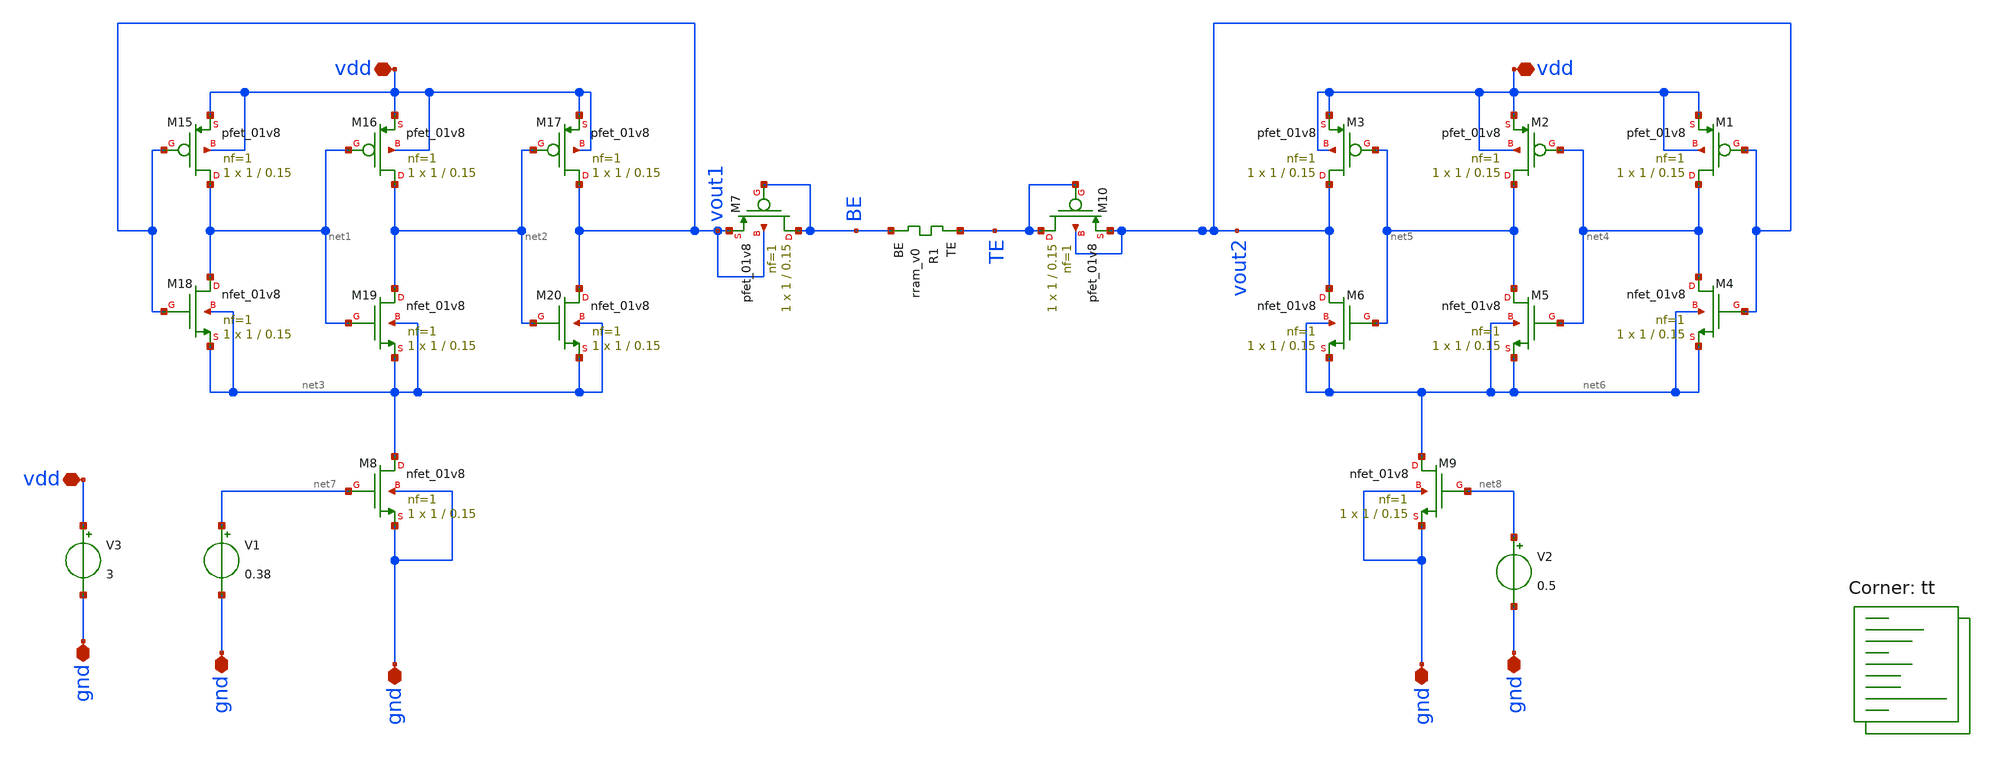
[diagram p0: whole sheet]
** sch_path: Neuron/voltContrOsc/sch/tb_vco_v2.sch
**.subckt tb_vco_v2 vdd vdd gnd gnd gnd gnd gnd vdd
*.iopin vdd
*.iopin vdd
*.iopin gnd
*.iopin gnd
*.iopin gnd
*.iopin gnd
*.iopin gnd
*.iopin vdd
XM15 net1 vout1 vdd vdd sky130_fd_pr__pfet_01v8 L=0.15 W=1 nf=1 ad='int((nf+1)/2) * W/nf * 0.29' as='int((nf+2)/2) * W/nf * 0.29'
+ pd='2*int((nf+1)/2) * (W/nf + 0.29)' ps='2*int((nf+2)/2) * (W/nf + 0.29)' nrd='0.29 / W' nrs='0.29 / W'
+ sa=0 sb=0 sd=0 mult=1 m=1
XM16 net2 net1 vdd vdd sky130_fd_pr__pfet_01v8 L=0.15 W=1 nf=1 ad='int((nf+1)/2) * W/nf * 0.29' as='int((nf+2)/2) * W/nf * 0.29'
+ pd='2*int((nf+1)/2) * (W/nf + 0.29)' ps='2*int((nf+2)/2) * (W/nf + 0.29)' nrd='0.29 / W' nrs='0.29 / W'
+ sa=0 sb=0 sd=0 mult=1 m=1
XM17 vout1 net2 vdd vdd sky130_fd_pr__pfet_01v8 L=0.15 W=1 nf=1 ad='int((nf+1)/2) * W/nf * 0.29' as='int((nf+2)/2) * W/nf * 0.29'
+ pd='2*int((nf+1)/2) * (W/nf + 0.29)' ps='2*int((nf+2)/2) * (W/nf + 0.29)' nrd='0.29 / W' nrs='0.29 / W'
+ sa=0 sb=0 sd=0 mult=1 m=1
XM18 net1 vout1 net3 net3 sky130_fd_pr__nfet_01v8 L=0.15 W=1 nf=1 ad='int((nf+1)/2) * W/nf * 0.29' as='int((nf+2)/2) * W/nf * 0.29'
+ pd='2*int((nf+1)/2) * (W/nf + 0.29)' ps='2*int((nf+2)/2) * (W/nf + 0.29)' nrd='0.29 / W' nrs='0.29 / W'
+ sa=0 sb=0 sd=0 mult=1 m=1
XM19 net2 net1 net3 net3 sky130_fd_pr__nfet_01v8 L=0.15 W=1 nf=1 ad='int((nf+1)/2) * W/nf * 0.29' as='int((nf+2)/2) * W/nf * 0.29'
+ pd='2*int((nf+1)/2) * (W/nf + 0.29)' ps='2*int((nf+2)/2) * (W/nf + 0.29)' nrd='0.29 / W' nrs='0.29 / W'
+ sa=0 sb=0 sd=0 mult=1 m=1
XM20 vout1 net2 net3 net3 sky130_fd_pr__nfet_01v8 L=0.15 W=1 nf=1 ad='int((nf+1)/2) * W/nf * 0.29' as='int((nf+2)/2) * W/nf * 0.29'
+ pd='2*int((nf+1)/2) * (W/nf + 0.29)' ps='2*int((nf+2)/2) * (W/nf + 0.29)' nrd='0.29 / W' nrs='0.29 / W'
+ sa=0 sb=0 sd=0 mult=1 m=1
XM1 net4 vout2 vdd vdd sky130_fd_pr__pfet_01v8 L=0.15 W=1 nf=1 ad='int((nf+1)/2) * W/nf * 0.29' as='int((nf+2)/2) * W/nf * 0.29'
+ pd='2*int((nf+1)/2) * (W/nf + 0.29)' ps='2*int((nf+2)/2) * (W/nf + 0.29)' nrd='0.29 / W' nrs='0.29 / W'
+ sa=0 sb=0 sd=0 mult=1 m=1
XM2 net5 net4 vdd vdd sky130_fd_pr__pfet_01v8 L=0.15 W=1 nf=1 ad='int((nf+1)/2) * W/nf * 0.29' as='int((nf+2)/2) * W/nf * 0.29'
+ pd='2*int((nf+1)/2) * (W/nf + 0.29)' ps='2*int((nf+2)/2) * (W/nf + 0.29)' nrd='0.29 / W' nrs='0.29 / W'
+ sa=0 sb=0 sd=0 mult=1 m=1
XM3 vout2 net5 vdd vdd sky130_fd_pr__pfet_01v8 L=0.15 W=1 nf=1 ad='int((nf+1)/2) * W/nf * 0.29' as='int((nf+2)/2) * W/nf * 0.29'
+ pd='2*int((nf+1)/2) * (W/nf + 0.29)' ps='2*int((nf+2)/2) * (W/nf + 0.29)' nrd='0.29 / W' nrs='0.29 / W'
+ sa=0 sb=0 sd=0 mult=1 m=1
XM4 net4 vout2 net6 net6 sky130_fd_pr__nfet_01v8 L=0.15 W=1 nf=1 ad='int((nf+1)/2) * W/nf * 0.29' as='int((nf+2)/2) * W/nf * 0.29'
+ pd='2*int((nf+1)/2) * (W/nf + 0.29)' ps='2*int((nf+2)/2) * (W/nf + 0.29)' nrd='0.29 / W' nrs='0.29 / W'
+ sa=0 sb=0 sd=0 mult=1 m=1
XM5 net5 net4 net6 net6 sky130_fd_pr__nfet_01v8 L=0.15 W=1 nf=1 ad='int((nf+1)/2) * W/nf * 0.29' as='int((nf+2)/2) * W/nf * 0.29'
+ pd='2*int((nf+1)/2) * (W/nf + 0.29)' ps='2*int((nf+2)/2) * (W/nf + 0.29)' nrd='0.29 / W' nrs='0.29 / W'
+ sa=0 sb=0 sd=0 mult=1 m=1
XM6 vout2 net5 net6 net6 sky130_fd_pr__nfet_01v8 L=0.15 W=1 nf=1 ad='int((nf+1)/2) * W/nf * 0.29' as='int((nf+2)/2) * W/nf * 0.29'
+ pd='2*int((nf+1)/2) * (W/nf + 0.29)' ps='2*int((nf+2)/2) * (W/nf + 0.29)' nrd='0.29 / W' nrs='0.29 / W'
+ sa=0 sb=0 sd=0 mult=1 m=1
XR1 TE BE rram_v0
XM8 net3 net7 gnd gnd sky130_fd_pr__nfet_01v8 L=0.15 W=1 nf=1 ad='int((nf+1)/2) * W/nf * 0.29' as='int((nf+2)/2) * W/nf * 0.29'
+ pd='2*int((nf+1)/2) * (W/nf + 0.29)' ps='2*int((nf+2)/2) * (W/nf + 0.29)' nrd='0.29 / W' nrs='0.29 / W'
+ sa=0 sb=0 sd=0 mult=1 m=1
XM9 net6 net8 gnd gnd sky130_fd_pr__nfet_01v8 L=0.15 W=1 nf=1 ad='int((nf+1)/2) * W/nf * 0.29' as='int((nf+2)/2) * W/nf * 0.29'
+ pd='2*int((nf+1)/2) * (W/nf + 0.29)' ps='2*int((nf+2)/2) * (W/nf + 0.29)' nrd='0.29 / W' nrs='0.29 / W'
+ sa=0 sb=0 sd=0 mult=1 m=1
V1 net7 gnd 0.38
V2 net8 gnd 0.5
V3 vdd gnd 3
XM7 BE BE vout1 vout1 sky130_fd_pr__pfet_01v8 L=0.15 W=1 nf=1 ad='int((nf+1)/2) * W/nf * 0.29' as='int((nf+2)/2) * W/nf * 0.29'
+ pd='2*int((nf+1)/2) * (W/nf + 0.29)' ps='2*int((nf+2)/2) * (W/nf + 0.29)' nrd='0.29 / W' nrs='0.29 / W'
+ sa=0 sb=0 sd=0 mult=1 m=1
XM10 TE TE vout2 vout2 sky130_fd_pr__pfet_01v8 L=0.15 W=1 nf=1 ad='int((nf+1)/2) * W/nf * 0.29' as='int((nf+2)/2) * W/nf * 0.29'
+ pd='2*int((nf+1)/2) * (W/nf + 0.29)' ps='2*int((nf+2)/2) * (W/nf + 0.29)' nrd='0.29 / W' nrs='0.29 / W'
+ sa=0 sb=0 sd=0 mult=1 m=1
**** begin user architecture code


.control
  * Modify according to your specific location
  save all
  tran 1n 10u
  write tb_vco_v2.raw
.endc




** opencircuitdesign pdks install
.inc $::SKYWATER_MODELS/rram_v0.spice

.lib $::SKYWATER_MODELS/sky130.lib.spice tt
**** end user architecture code
**.ends
.end
